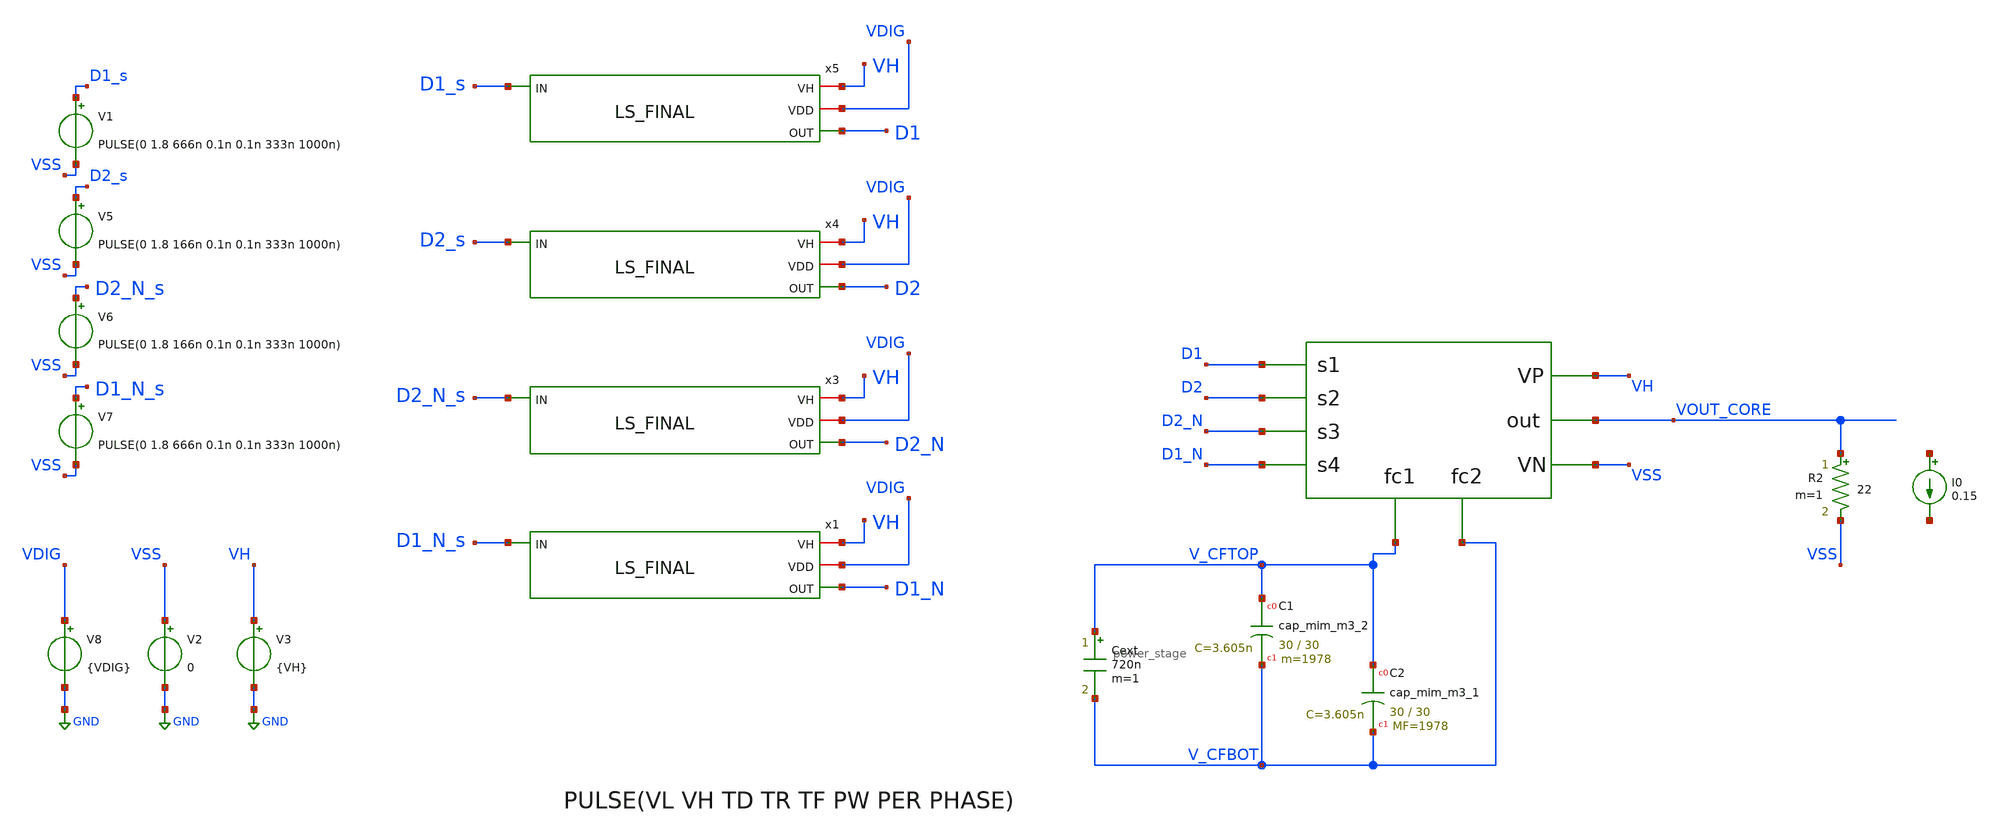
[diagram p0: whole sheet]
** sch_path: xschem/testbench/Interleaved/pulsos_jm.sch
**.subckt pulsos_jm
V2 VSS GND 0
V3 VH GND {VH}
I0 net1 net2 0.15
R2 VOUT_CORE VSS 22 m=1
XC1 V_CFTOP V_CFBOT sky130_fd_pr__cap_mim_m3_2 W=30 L=30 MF=1978 m=1978
XC2 V_CFTOP V_CFBOT sky130_fd_pr__cap_mim_m3_1 W=30 L=30 MF=1978 m=1978
X2 D1 D2 D2_N D1_N V_CFTOP V_CFBOT VOUT_CORE VH VSS power_stage
Cext V_CFTOP V_CFBOT 720n m=1
x1 VH VDIG D1_N D1_N_s LS_FINAL
V8 VDIG GND {VDIG}
x3 VH VDIG D2_N D2_N_s LS_FINAL
V6 D2_N_s VSS PULSE(0 1.8 166n 0.1n 0.1n 333n 1000n)
V5 D2_s VSS PULSE(0 1.8 166n 0.1n 0.1n 333n 1000n)
V7 D1_N_s VSS PULSE(0 1.8 666n 0.1n 0.1n 333n 1000n)
V1 D1_s VSS PULSE(0 1.8 666n 0.1n 0.1n 333n 1000n)
x4 VH VDIG D2 D2_s LS_FINAL
x5 VH VDIG D1 D1_s LS_FINAL
**** begin user architecture code


.param VIN = 5
.param VDIG = 1.8
.param VH = 5
.param RL = 50
.option scale=1e-6
*.option temp=70
.ic v(V_CFTOP) = VH/2
.ic v(vout_core)=0
.ic v(V_CFBOT) = 0
*.probe vd(MP2:G:S)
*.save all
*.save v(d1) v(d2) v(d1top_5v) v(d2_5v) v(d2bot_5v) v(d1bot_5v) v(vout) v(vout_core) v(vdd) v(vh) i(v1) i(v5) i(vmeas) v(v_cftop,v_cfbot)
.save v(D1) v(D2) v(D1_N) v(D2_N) v(VOUT_CORE) v(vh) i(v3) v(v_cftop,v_cfbot) v(D1,v_cftop) v(D2,vout_core) v(D2_N,v_cfbot) v(D1_Nv,VSS) v(v_out_ls1) v(v_out_ls2) v(d2_n,v_cfbot)
.save @m.xm4.msky130_fd_pr__nfet_g5v0d10v5[vds]
.param mc_mm_switch=0
*.lib /home/jorge/Documents/Postdoc/share/pdk/sky130A/libs.tech/ngspice/sky130.lib.spice tt
*.lib /usr/share/pdk/sky130A/libs.tech/ngspice/sky130.lib.spice ss
.lib /foss/pdk/sky130A/libs.tech/ngspice/sky130.lib.spice TT
*.include /usr/share/pdk/sky130A/libs.ref/sky130_fd_sc_hvl/spice/sky130_fd_sc_hvl.spice
*.include /home/jorge/Documents/Postdoc/share/pdk/sky130A/libs.ref/sky130_fd_sc_hvl/spice/sky130_fd_sc_hvl.spice
.options savecurrents
.control
*save all
tran 100n 3u
*write DCDC_v1p4_5MHz_NMOS_PMOS.raw
*wrdata
*+ ~/Documents/Postdoc/chipathon2022/3LFCC_AC3E/xschem/dev_switches/DCDC_5V_FINAL/3LFCC_v1p4.txt tran.v(vout) tran.i(vmeas) tran.v(vdd) tran.i(v3) tran.v(vh) tran.i(v5)
*wrdata /foss/designs/personal/3LFCC_AC3E/xschem/hierarchy_sch/DCDC_5V_FINAL/3LFCC_v1p4.txt
*+ tran.v(vout_core) tran.i(v1)
wrdata /foss/designs/3LFCC_AC3E/xschem/hierarchy_sch/DCDC_5V_FINAL/3LFCC_v1p4_LSH2_jm.txt
+ tran.v(vout_core) tran.i(v3)


**plot v(d1top_5v) v(d2_5v)
**plot v(d2bot_5v) v(d1bot_5v)
plot v(v_cftop,v_cfbot) v(vout_core)
plot v(D1,VH) v(D1_N,VSS)
plot v(D2,V_CFTOP) v(D2_N,V_CFBOT)
plot  v(vout_core)
plot i(v3) v(D1,VH) v(D1_N,VSS)
plot i(v3) v(D2,V_CFTOP) v(D2_N,V_CFBOT)
**plot i(v1)
plot i(v3) v(v_cftop,v_cfbot)
**plot @m.xm4.msky130_fd_pr__nfet_g5v0d10v5[vds]
plot v(v_out_ls1) v(d1_n)
plot v(v_out_ls2) v(d2_n,v_cfbot)


*plot v(d1top_5v) v(d2_5v) v(d2bot_5v) v(d1bot_5v) v(v_cftop,v_cfbot) v(vout)
*plot v(v_cftop,v_cfbot) v(vout)
.endc


**** end user architecture code
**.ends

* expanding   symbol:  /foss/designs/3LFCC_AC3E/xschem/hierarchy_sch/power_stage.sym # of pins=9
** sym_path: xschem/hierarchy_sch/power_stage.sym
** sch_path: xschem/hierarchy_sch/power_stage.sch
.subckt power_stage s1 s2 s3 s4 fc1 fc2 out VP VN
*.ipin s1
*.ipin s2
*.ipin s3
*.ipin s4
*.iopin VP
*.iopin VN
*.opin out
*.opin fc1
*.opin fc2
X1 s2 fc1 s1 VP out transistor_group_one
X2 s4 fc2 s3 out VN transistor_group_two
.ends


* expanding   symbol:  /foss/designs/3LFCC_AC3E/xschem/hierarchy_sch/Driver_UCU/sch/LS_FINAL.sym #
*+ of pins=4
** sym_path: xschem/hierarchy_sch/LS_FINAL.sym
** sch_path: xschem/hierarchy_sch/LS_FINAL.sch
.subckt LS_FINAL VH VDD OUT IN
*.ipin IN
*.iopin VDD
*.iopin VH
*.opin OUT
XM11 net1 IN VDD VDD sky130_fd_pr__pfet_01v8 L=0.15 W=1 nf=1 ad='int((nf+1)/2) * W/nf * 0.29' as='int((nf+2)/2) * W/nf * 0.29'
+ pd='2*int((nf+1)/2) * (W/nf + 0.29)' ps='2*int((nf+2)/2) * (W/nf + 0.29)' nrd='0.29 / W' nrs='0.29 / W'
+ sa=0 sb=0 sd=0 mult=5 m=5
XM12 net1 IN GND GND sky130_fd_pr__nfet_01v8 L=0.15 W=1 nf=1 ad='int((nf+1)/2) * W/nf * 0.29' as='int((nf+2)/2) * W/nf * 0.29'
+ pd='2*int((nf+1)/2) * (W/nf + 0.29)' ps='2*int((nf+2)/2) * (W/nf + 0.29)' nrd='0.29 / W' nrs='0.29 / W'
+ sa=0 sb=0 sd=0 mult=5 m=5
XM15 net2 net3 VH VH sky130_fd_pr__pfet_g5v0d10v5 L=0.5 W=2 nf=1 ad='int((nf+1)/2) * W/nf * 0.29' as='int((nf+2)/2) * W/nf * 0.29'
+ pd='2*int((nf+1)/2) * (W/nf + 0.29)' ps='2*int((nf+2)/2) * (W/nf + 0.29)' nrd='0.29 / W' nrs='0.29 / W'
+ sa=0 sb=0 sd=0 mult=1 m=1
XM14 net3 net2 VH VH sky130_fd_pr__pfet_g5v0d10v5 L=0.5 W=2 nf=1 ad='int((nf+1)/2) * W/nf * 0.29' as='int((nf+2)/2) * W/nf * 0.29'
+ pd='2*int((nf+1)/2) * (W/nf + 0.29)' ps='2*int((nf+2)/2) * (W/nf + 0.29)' nrd='0.29 / W' nrs='0.29 / W'
+ sa=0 sb=0 sd=0 mult=1 m=1
XM16 net4 net2 VH VH sky130_fd_pr__pfet_g5v0d10v5 L=0.5 W=10 nf=1 ad='int((nf+1)/2) * W/nf * 0.29' as='int((nf+2)/2) * W/nf * 0.29'
+ pd='2*int((nf+1)/2) * (W/nf + 0.29)' ps='2*int((nf+2)/2) * (W/nf + 0.29)' nrd='0.29 / W' nrs='0.29 / W'
+ sa=0 sb=0 sd=0 mult=10 m=10
XM18 net2 net1 GND GND sky130_fd_pr__nfet_g5v0d10v5 L=0.5 W=4 nf=1 ad='int((nf+1)/2) * W/nf * 0.29' as='int((nf+2)/2) * W/nf * 0.29'
+ pd='2*int((nf+1)/2) * (W/nf + 0.29)' ps='2*int((nf+2)/2) * (W/nf + 0.29)' nrd='0.29 / W' nrs='0.29 / W'
+ sa=0 sb=0 sd=0 mult=3 m=3
XM13 net3 IN GND GND sky130_fd_pr__nfet_g5v0d10v5 L=0.5 W=4 nf=1 ad='int((nf+1)/2) * W/nf * 0.29' as='int((nf+2)/2) * W/nf * 0.29'
+ pd='2*int((nf+1)/2) * (W/nf + 0.29)' ps='2*int((nf+2)/2) * (W/nf + 0.29)' nrd='0.29 / W' nrs='0.29 / W'
+ sa=0 sb=0 sd=0 mult=3 m=3
XM17 net4 IN GND GND sky130_fd_pr__nfet_g5v0d10v5 L=0.5 W=10 nf=1 ad='int((nf+1)/2) * W/nf * 0.29' as='int((nf+2)/2) * W/nf * 0.29'
+ pd='2*int((nf+1)/2) * (W/nf + 0.29)' ps='2*int((nf+2)/2) * (W/nf + 0.29)' nrd='0.29 / W' nrs='0.29 / W'
+ sa=0 sb=0 sd=0 mult=10 m=10
XM7 OUT net4 VH VH sky130_fd_pr__pfet_g5v0d10v5 L=0.5 W=20 nf=1 ad='int((nf+1)/2) * W/nf * 0.29' as='int((nf+2)/2) * W/nf * 0.29'
+ pd='2*int((nf+1)/2) * (W/nf + 0.29)' ps='2*int((nf+2)/2) * (W/nf + 0.29)' nrd='0.29 / W' nrs='0.29 / W'
+ sa=0 sb=0 sd=0 mult=20 m=20
XM10 OUT net4 GND GND sky130_fd_pr__nfet_g5v0d10v5 L=0.5 W=20 nf=1 ad='int((nf+1)/2) * W/nf * 0.29' as='int((nf+2)/2) * W/nf * 0.29'
+ pd='2*int((nf+1)/2) * (W/nf + 0.29)' ps='2*int((nf+2)/2) * (W/nf + 0.29)' nrd='0.29 / W' nrs='0.29 / W'
+ sa=0 sb=0 sd=0 mult=20 m=20
.ends


* expanding   symbol:  personal/3LFCC_AC3E/xschem/hierarchy_sch/transistor_group_one.sym # of pins=5
** sym_path: xschem/hierarchy_sch/transistor_group_one.sym
** sch_path: xschem/hierarchy_sch/transistor_group_one.sch
.subckt transistor_group_one s2 fc1 s1 VP out
*.iopin VP
*.ipin s1
*.ipin s2
*.opin fc1
*.iopin out
XM3 out s2 fc1 fc1 sky130_fd_pr__pfet_g5v0d10v5 L=0.5 W=4.38 nf=1 ad='int((nf+1)/2) * W/nf * 0.29' as='int((nf+2)/2) * W/nf * 0.29'
+ pd='2*int((nf+1)/2) * (W/nf + 0.29)' ps='2*int((nf+2)/2) * (W/nf + 0.29)' nrd='0.29 / W' nrs='0.29 / W'
+ sa=0 sb=0 sd=0 mult=4506 m=4506
XM4 fc1 s1 VP VP sky130_fd_pr__pfet_g5v0d10v5 L=0.5 W=4.38 nf=1 ad='int((nf+1)/2) * W/nf * 0.29' as='int((nf+2)/2) * W/nf * 0.29'
+ pd='2*int((nf+1)/2) * (W/nf + 0.29)' ps='2*int((nf+2)/2) * (W/nf + 0.29)' nrd='0.29 / W' nrs='0.29 / W'
+ sa=0 sb=0 sd=0 mult=4506 m=4506
.ends


* expanding   symbol:  personal/3LFCC_AC3E/xschem/hierarchy_sch/transistor_group_two.sym # of pins=5
** sym_path: xschem/hierarchy_sch/transistor_group_two.sym
** sch_path: xschem/hierarchy_sch/transistor_group_two.sch
.subckt transistor_group_two s4 fc2 s3 out VN
*.iopin out
*.ipin s3
*.ipin s4
*.opin fc2
*.iopin VN
XM1 out s3 fc2 fc2 sky130_fd_pr__nfet_g5v0d10v5 L=0.5 W=4.38 nf=1 ad='int((nf+1)/2) * W/nf * 0.29' as='int((nf+2)/2) * W/nf * 0.29'
+ pd='2*int((nf+1)/2) * (W/nf + 0.29)' ps='2*int((nf+2)/2) * (W/nf + 0.29)' nrd='0.29 / W' nrs='0.29 / W'
+ sa=0 sb=0 sd=0 mult=2520 m=2520
XM2 fc2 s4 VN VN sky130_fd_pr__nfet_g5v0d10v5 L=0.5 W=4.38 nf=1 ad='int((nf+1)/2) * W/nf * 0.29' as='int((nf+2)/2) * W/nf * 0.29'
+ pd='2*int((nf+1)/2) * (W/nf + 0.29)' ps='2*int((nf+2)/2) * (W/nf + 0.29)' nrd='0.29 / W' nrs='0.29 / W'
+ sa=0 sb=0 sd=0 mult=2520 m=2520
.ends

.GLOBAL GND
.end
